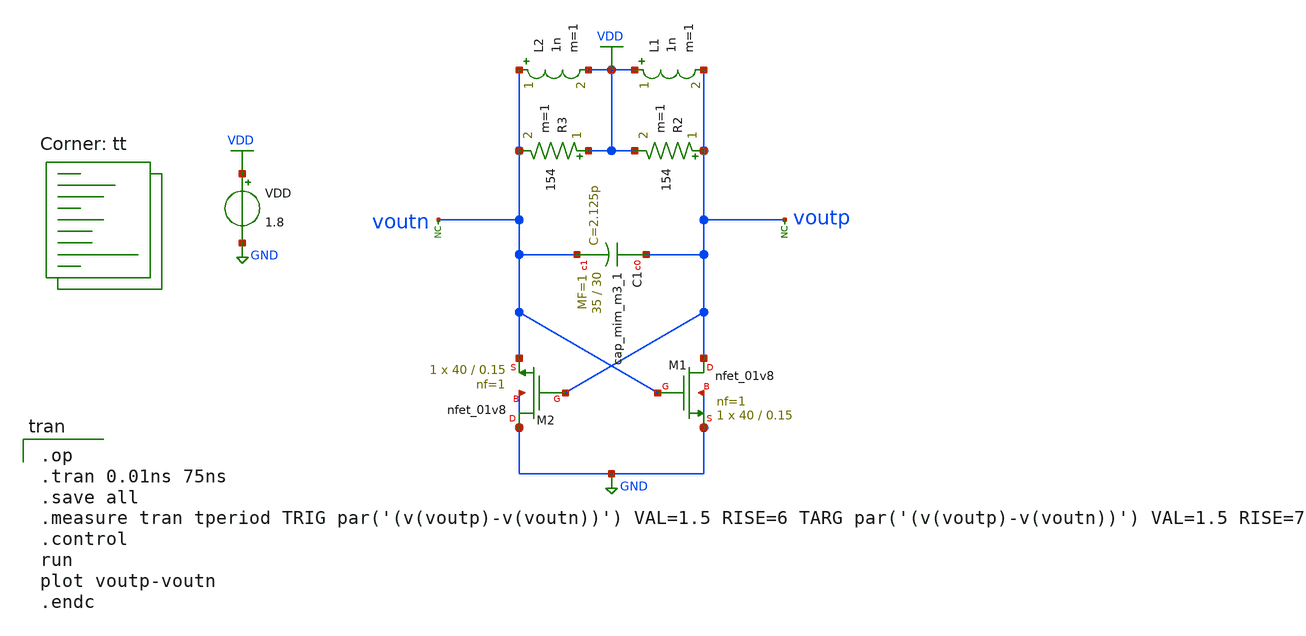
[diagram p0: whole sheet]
** sch_path: pll/lc_vco_lib_Ahmed_Elshahat/NMOS_OSC_tb/xschem/NMOS_OSC.sch
**.subckt NMOS_OSC
L1 VDD voutp 1n m=1
R2 voutp VDD 154 m=1
L2 voutn VDD 1n m=1
R3 VDD voutn 154 m=1
XC1 voutp voutn sky130_fd_pr__cap_mim_m3_1 W=35 L=30 MF=1 m=1
XM2 GND voutp voutn GND sky130_fd_pr__nfet_01v8 L=0.15 W=40 nf=1 ad='int((1 + 1)/2) * 40 / 1 * 0.29'
+ as='int((1 + 2)/2) * 40 / 1 * 0.29' pd='2*int((1 + 1)/2) * (40 / 1 + 0.29)' ps='2*int((1 + 2)/2) * (40 / 1 + 0.29)'
+ nrd='0.29 / 40 ' nrs='0.29 / 40 ' sa=0 sb=0 sd=0 mult=1 m=1
XM1 voutp voutn GND GND sky130_fd_pr__nfet_01v8 L=0.15 W=40 nf=1 ad='int((1 + 1)/2) * 40 / 1 * 0.29'
+ as='int((1 + 2)/2) * 40 / 1 * 0.29' pd='2*int((1 + 1)/2) * (40 / 1 + 0.29)' ps='2*int((1 + 2)/2) * (40 / 1 + 0.29)'
+ nrd='0.29 / 40 ' nrs='0.29 / 40 ' sa=0 sb=0 sd=0 mult=1 m=1
* noconn voutp
* noconn voutp
* noconn voutn
VDD VDD GND 1.8
**** begin user architecture code

.op
.tran 0.01ns 75ns
.save all
.measure tran tperiod TRIG par('(v(voutp)-v(voutn))') VAL=1.5 RISE=6 TARG par('(v(voutp)-v(voutn))')
+ VAL=1.5 RISE=7
.control
run
plot voutp-voutn
.endc

.lib $::SKYWATER_MODELS/sky130.lib.spice tt

** opencircuitdesign pdks install
.lib $::SKYWATER_MODELS/sky130.lib.spice tt


**** end user architecture code
**.ends
.GLOBAL VDD
.GLOBAL GND
.end
